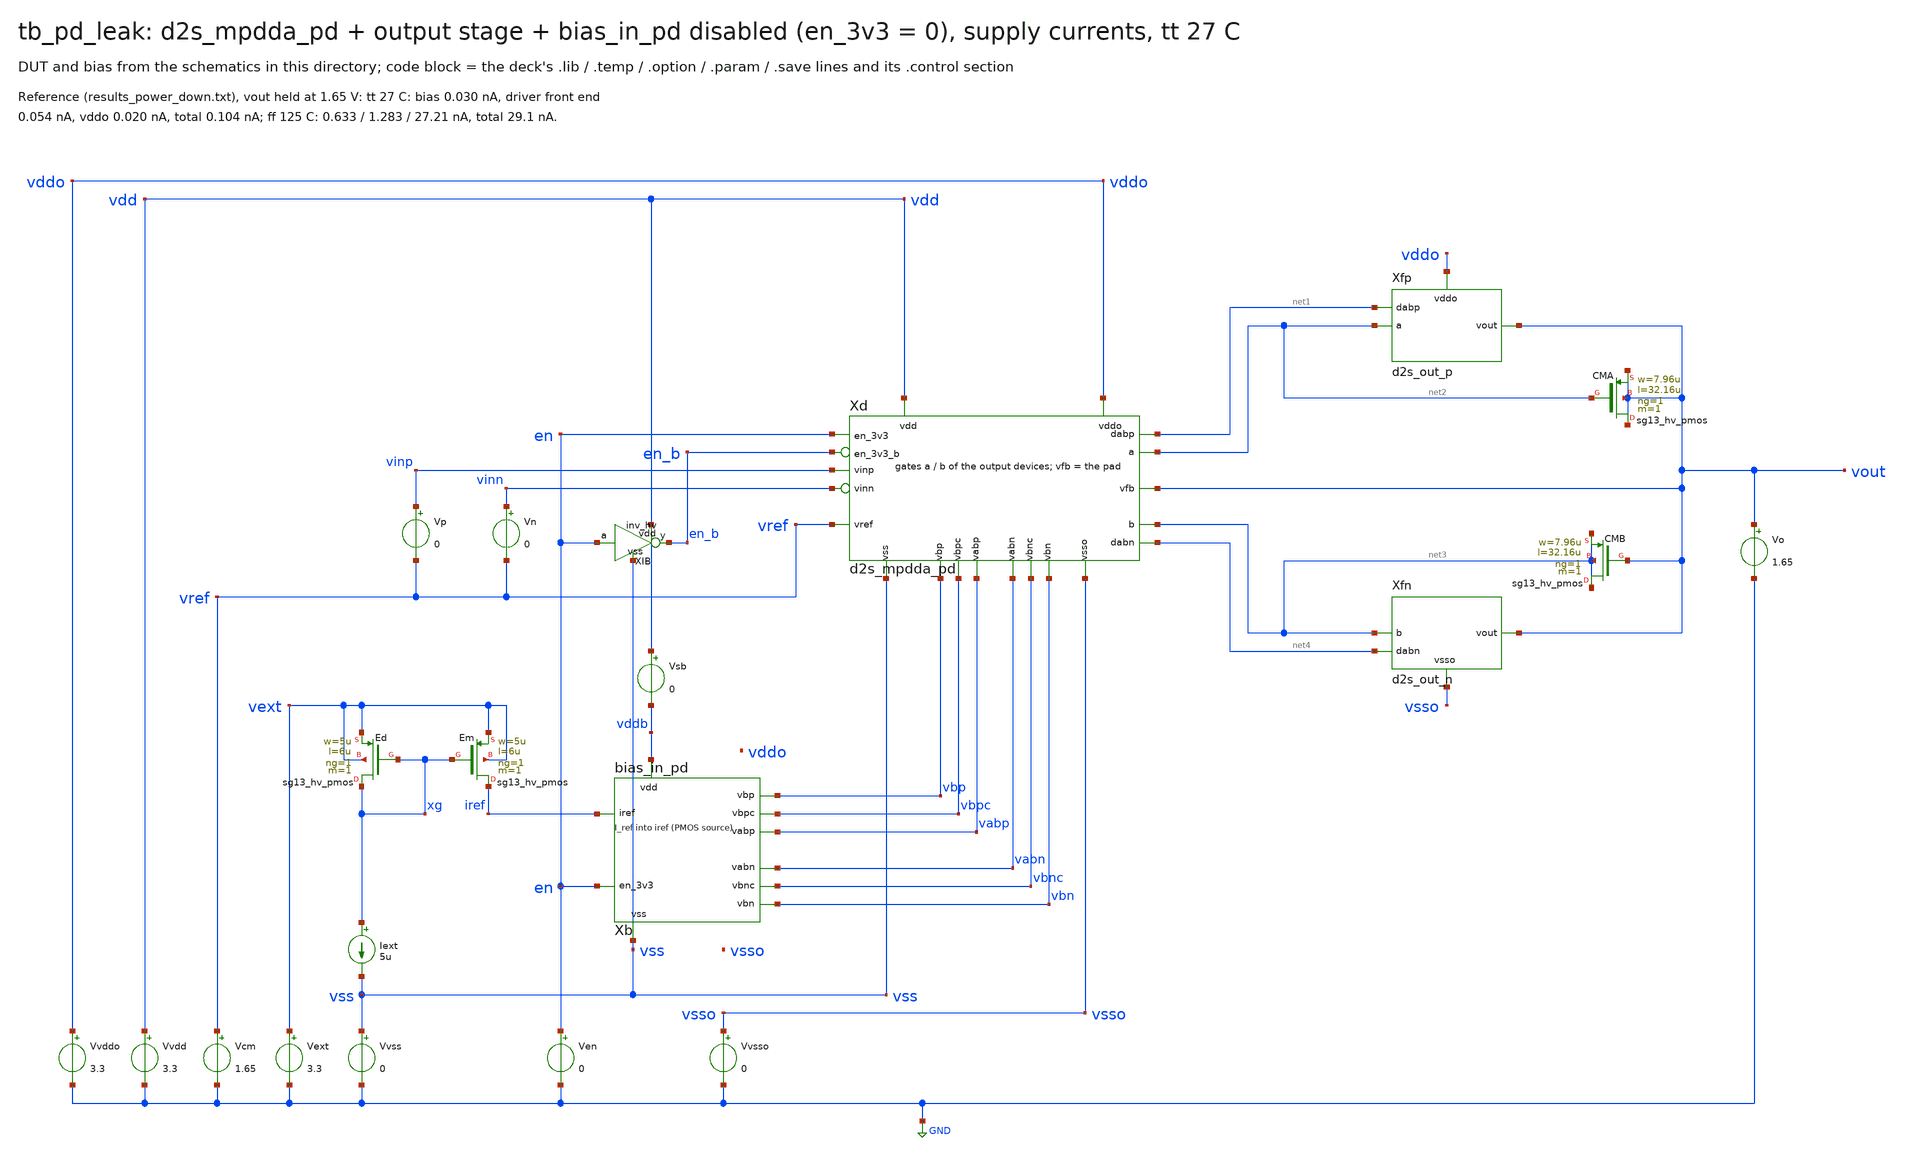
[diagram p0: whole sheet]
** sch_path: macros/sg13cmos5l_IOPadDiff2Single/testbenches/xschem/tb_pd_leak.sch
**.subckt tb_pd_leak
Vvdd vdd GND 3.3
Vvss vss GND 0
Vvddo vddo GND 3.3
Vvsso vsso GND 0
Ven en GND 0
Vext vext GND 3.3
Vcm vref GND 1.65
Xb vddb vss iref vbp vbn vbpc vbnc vabp vabn en bias_in_pd
Xd vdd vss vddo vsso vinp vinn vref vout net2 net3 net1 net4 vbp vbn vbpc vbnc vabp vabn en en_b
+ d2s_mpdda_pd
Vp vinp vref 0
Vn vinn vref 0
XEd xg xg vext vext sg13_hv_pmos w=5u l=6u ng=1 m=1 mm_ok=1
XEm iref xg vext vext sg13_hv_pmos w=5u l=6u ng=1 m=1 mm_ok=1
Iext xg vss 5u
Vsb vdd vddb 0
Vo vout GND 1.65
XIB vdd vss en en_b inv_hv
Xfp vddo net2 vout net1 d2s_out_p
Xfn vsso net3 vout net4 d2s_out_n
XCMA vout net2 vout vout sg13_hv_pmos w=7.96u l=32.16u ng=1 m=1 mm_ok=1
XCMB net3 vout net3 net3 sg13_hv_pmos w=7.96u l=32.16u ng=1 m=1 mm_ok=1
**** begin user architecture code

.lib cornerMOShv.lib mos_tt
.lib cornerRES.lib res_typ
.lib cornerCAP.lib cap_typ
.temp 27
.control
op
let ibias = i(vsb)
let idrv = -i(vvdd) - i(vsb)
let iddo = -i(vvddo)
let itot = -i(vvdd) - i(vvddo)
let vsg_op = v(vddo) - v(a)
let vgs_on = v(b) - v(vsso)
print ibias idrv iddo itot vsg_op vgs_on
print v(vbp) v(vbpc) v(vabp) v(vabn) v(vbn) v(vbnc)
.endc

**** end user architecture code
**.ends
.GLOBAL GND
.end
